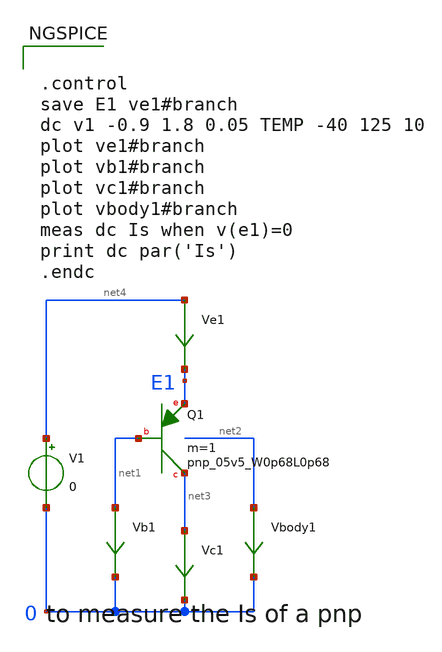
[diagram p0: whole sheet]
** sch_path: schematics/bipolar_characterization_scale_current.sch
**.subckt bipolar_characterization_scale_current
XQ1 net3 net1 E1 sky130_fd_pr__pnp_05v5_W0p68L0p68 m=1
V1 net4 0 0
Ve1 net4 E1 0
.save i(ve1)
Vc1 net3 0 0
.save i(vc1)
Vb1 net1 0 0
.save i(vb1)
Vbody1 net2 0 0
.save i(vbody1)
**** begin user architecture code


.control
save E1 ve1#branch
dc v1 -0.9 1.8 0.05 TEMP -40 125 10
plot ve1#branch
plot vb1#branch
plot vc1#branch
plot vbody1#branch
meas dc Is when v(e1)=0
print dc par('Is')
.endc



.include $::SKYWATER_MODELS/cells/nfet_01v8/sky130_fd_pr__nfet_01v8__tt.corner.spice
.include $::SKYWATER_MODELS/cells/nfet_01v8_lvt/sky130_fd_pr__nfet_01v8_lvt__tt.corner.spice
.include $::SKYWATER_MODELS/cells/pfet_01v8/sky130_fd_pr__pfet_01v8__tt.corner.spice
.include $::SKYWATER_MODELS/cells/nfet_03v3_nvt/sky130_fd_pr__nfet_03v3_nvt__tt.corner.spice
.include $::SKYWATER_MODELS/cells/nfet_05v0_nvt/sky130_fd_pr__nfet_05v0_nvt__tt.corner.spice
.include $::SKYWATER_MODELS/cells/esd_nfet_01v8/sky130_fd_pr__esd_nfet_01v8__tt.corner.spice
.include $::SKYWATER_MODELS/cells/pfet_01v8_lvt/sky130_fd_pr__pfet_01v8_lvt__tt.corner.spice
.include $::SKYWATER_MODELS/cells/pfet_01v8_hvt/sky130_fd_pr__pfet_01v8_hvt__tt.corner.spice
.include $::SKYWATER_MODELS/cells/esd_pfet_g5v0d10v5/sky130_fd_pr__esd_pfet_g5v0d10v5__tt.corner.spice
.include $::SKYWATER_MODELS/cells/pfet_g5v0d10v5/sky130_fd_pr__pfet_g5v0d10v5__tt.corner.spice
.include $::SKYWATER_MODELS/cells/pfet_g5v0d16v0/sky130_fd_pr__pfet_g5v0d16v0__tt.corner.spice
.include $::SKYWATER_MODELS/cells/nfet_g5v0d10v5/sky130_fd_pr__nfet_g5v0d10v5__tt.corner.spice
.include $::SKYWATER_MODELS/cells/nfet_g5v0d16v0/sky130_fd_pr__nfet_g5v0d16v0__tt_discrete.corner.spice
.include $::SKYWATER_MODELS/cells/esd_nfet_g5v0d10v5/sky130_fd_pr__esd_nfet_g5v0d10v5__tt.corner.spice
.include $::SKYWATER_MODELS/models/corners/tt/nonfet.spice
* Mismatch parameters
.include $::SKYWATER_MODELS/cells/nfet_01v8/sky130_fd_pr__nfet_01v8__mismatch.corner.spice
.include $::SKYWATER_MODELS/cells/pfet_01v8/sky130_fd_pr__pfet_01v8__mismatch.corner.spice
.include $::SKYWATER_MODELS/cells/nfet_01v8_lvt/sky130_fd_pr__nfet_01v8_lvt__mismatch.corner.spice
.include $::SKYWATER_MODELS/cells/pfet_01v8_lvt/sky130_fd_pr__pfet_01v8_lvt__mismatch.corner.spice
.include $::SKYWATER_MODELS/cells/pfet_01v8_hvt/sky130_fd_pr__pfet_01v8_hvt__mismatch.corner.spice
.include $::SKYWATER_MODELS/cells/nfet_g5v0d10v5/sky130_fd_pr__nfet_g5v0d10v5__mismatch.corner.spice
.include $::SKYWATER_MODELS/cells/pfet_g5v0d10v5/sky130_fd_pr__pfet_g5v0d10v5__mismatch.corner.spice
.include $::SKYWATER_MODELS/cells/nfet_05v0_nvt/sky130_fd_pr__nfet_05v0_nvt__mismatch.corner.spice
.include $::SKYWATER_MODELS/cells/nfet_03v3_nvt/sky130_fd_pr__nfet_03v3_nvt__mismatch.corner.spice
* Resistor$::SKYWATER_MODELS/Capacitor
.include $::SKYWATER_MODELS/models/r+c/res_typical__cap_typical.spice
.include $::SKYWATER_MODELS/models/r+c/res_typical__cap_typical__lin.spice
* Special cells
.include $::SKYWATER_MODELS/models/corners/tt/specialized_cells.spice
* All models
.include $::SKYWATER_MODELS/models/all.spice
* Corner
.include $::SKYWATER_MODELS/models/corners/tt/rf.spice

**** end user architecture code
**.ends
.end
